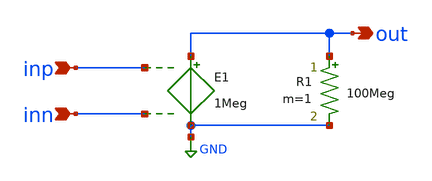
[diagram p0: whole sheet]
** sch_path: DSM_2ndOrder/1_Schematics/Ideal_Schematic/xschem/ideal_opamp.sch
**.subckt ideal_opamp out inp inn
*.opin out
*.ipin inp
*.ipin inn
E1 out GND inp inn 1Meg
R1 out GND 100Meg m=1
**.ends
.GLOBAL GND
.end
